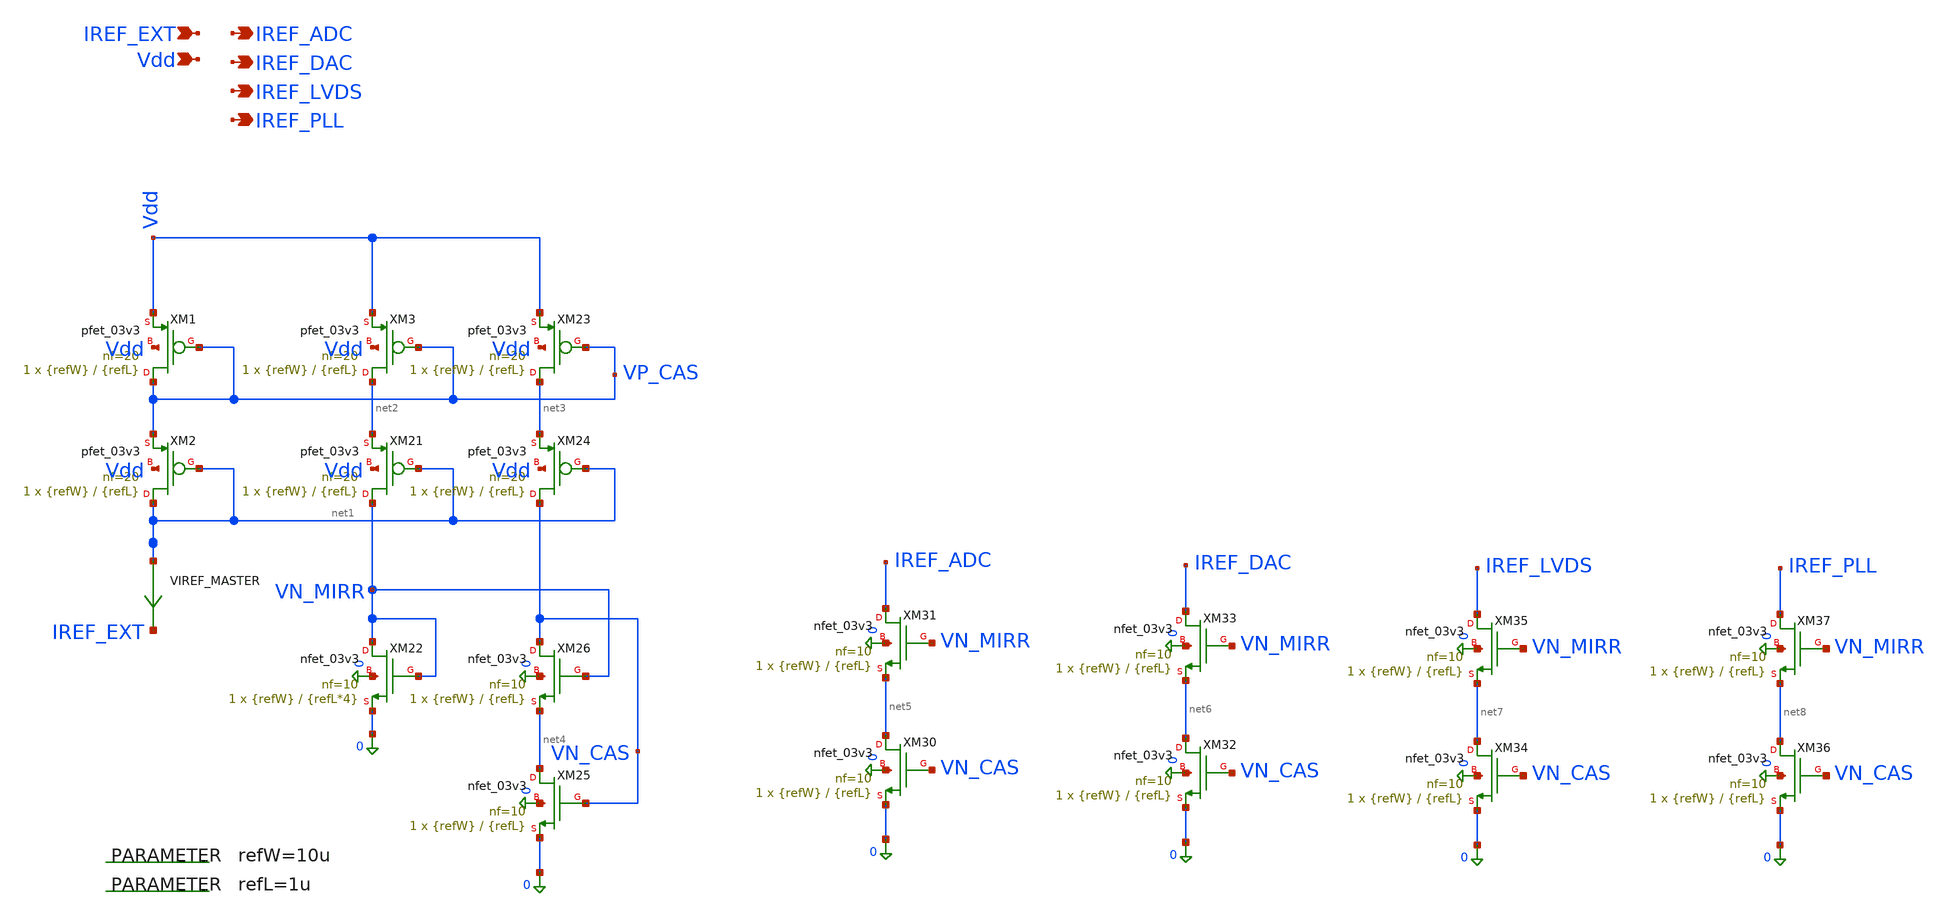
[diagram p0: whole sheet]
** sch_path: blocks/top/iref_master.sch
**.subckt iref_master IREF_ADC IREF_DAC Vdd IREF_EXT IREF_LVDS IREF_PLL
*.opin IREF_ADC
*.opin IREF_DAC
*.ipin Vdd
*.ipin IREF_EXT
*.opin IREF_LVDS
*.opin IREF_PLL
XM1 VP_CAS VP_CAS Vdd Vdd pfet_03v3 L={refL} W={refW} nf=20 ad='int((nf+1)/2) * W/nf * 0.18u' as='int((nf+2)/2) * W/nf * 0.18u'
+ pd='2*int((nf+1)/2) * (W/nf + 0.18u)' ps='2*int((nf+2)/2) * (W/nf + 0.18u)' nrd='0.18u / W' nrs='0.18u / W'
+ sa=0 sb=0 sd=0 m=1
XM2 net1 net1 VP_CAS Vdd pfet_03v3 L={refL} W={refW} nf=20 ad='int((nf+1)/2) * W/nf * 0.18u' as='int((nf+2)/2) * W/nf * 0.18u'
+ pd='2*int((nf+1)/2) * (W/nf + 0.18u)' ps='2*int((nf+2)/2) * (W/nf + 0.18u)' nrd='0.18u / W' nrs='0.18u / W'
+ sa=0 sb=0 sd=0 m=1
XM3 net2 VP_CAS Vdd Vdd pfet_03v3 L={refL} W={refW} nf=20 ad='int((nf+1)/2) * W/nf * 0.18u' as='int((nf+2)/2) * W/nf * 0.18u'
+ pd='2*int((nf+1)/2) * (W/nf + 0.18u)' ps='2*int((nf+2)/2) * (W/nf + 0.18u)' nrd='0.18u / W' nrs='0.18u / W'
+ sa=0 sb=0 sd=0 m=1
XM21 VN_MIRR net1 net2 Vdd pfet_03v3 L={refL} W={refW} nf=20 ad='int((nf+1)/2) * W/nf * 0.18u' as='int((nf+2)/2) * W/nf * 0.18u'
+ pd='2*int((nf+1)/2) * (W/nf + 0.18u)' ps='2*int((nf+2)/2) * (W/nf + 0.18u)' nrd='0.18u / W' nrs='0.18u / W'
+ sa=0 sb=0 sd=0 m=1
XM22 VN_MIRR VN_MIRR 0 0 nfet_03v3 L={refL*4} W={refW} nf=10 ad='int((nf+1)/2) * W/nf * 0.18u' as='int((nf+2)/2) * W/nf * 0.18u'
+ pd='2*int((nf+1)/2) * (W/nf + 0.18u)' ps='2*int((nf+2)/2) * (W/nf + 0.18u)' nrd='0.18u / W' nrs='0.18u / W'
+ sa=0 sb=0 sd=0 m=1
XM23 net3 VP_CAS Vdd Vdd pfet_03v3 L={refL} W={refW} nf=20 ad='int((nf+1)/2) * W/nf * 0.18u' as='int((nf+2)/2) * W/nf * 0.18u'
+ pd='2*int((nf+1)/2) * (W/nf + 0.18u)' ps='2*int((nf+2)/2) * (W/nf + 0.18u)' nrd='0.18u / W' nrs='0.18u / W'
+ sa=0 sb=0 sd=0 m=1
XM24 VN_CAS net1 net3 Vdd pfet_03v3 L={refL} W={refW} nf=20 ad='int((nf+1)/2) * W/nf * 0.18u' as='int((nf+2)/2) * W/nf * 0.18u'
+ pd='2*int((nf+1)/2) * (W/nf + 0.18u)' ps='2*int((nf+2)/2) * (W/nf + 0.18u)' nrd='0.18u / W' nrs='0.18u / W'
+ sa=0 sb=0 sd=0 m=1
XM25 net4 VN_CAS 0 0 nfet_03v3 L={refL} W={refW} nf=10 ad='int((nf+1)/2) * W/nf * 0.18u' as='int((nf+2)/2) * W/nf * 0.18u'
+ pd='2*int((nf+1)/2) * (W/nf + 0.18u)' ps='2*int((nf+2)/2) * (W/nf + 0.18u)' nrd='0.18u / W' nrs='0.18u / W'
+ sa=0 sb=0 sd=0 m=1
XM26 VN_CAS VN_MIRR net4 0 nfet_03v3 L={refL} W={refW} nf=10 ad='int((nf+1)/2) * W/nf * 0.18u' as='int((nf+2)/2) * W/nf * 0.18u'
+ pd='2*int((nf+1)/2) * (W/nf + 0.18u)' ps='2*int((nf+2)/2) * (W/nf + 0.18u)' nrd='0.18u / W' nrs='0.18u / W'
+ sa=0 sb=0 sd=0 m=1
.param refW=10u
.param refL=1u
VIREF_MASTER net1 IREF_EXT 0
.save i(viref_master)
XM30 net5 VN_CAS 0 0 nfet_03v3 L={refL} W={refW} nf=10 ad='int((nf+1)/2) * W/nf * 0.18u' as='int((nf+2)/2) * W/nf * 0.18u'
+ pd='2*int((nf+1)/2) * (W/nf + 0.18u)' ps='2*int((nf+2)/2) * (W/nf + 0.18u)' nrd='0.18u / W' nrs='0.18u / W'
+ sa=0 sb=0 sd=0 m=1
XM31 IREF_ADC VN_MIRR net5 0 nfet_03v3 L={refL} W={refW} nf=10 ad='int((nf+1)/2) * W/nf * 0.18u' as='int((nf+2)/2) * W/nf * 0.18u'
+ pd='2*int((nf+1)/2) * (W/nf + 0.18u)' ps='2*int((nf+2)/2) * (W/nf + 0.18u)' nrd='0.18u / W' nrs='0.18u / W'
+ sa=0 sb=0 sd=0 m=1
XM32 net6 VN_CAS 0 0 nfet_03v3 L={refL} W={refW} nf=10 ad='int((nf+1)/2) * W/nf * 0.18u' as='int((nf+2)/2) * W/nf * 0.18u'
+ pd='2*int((nf+1)/2) * (W/nf + 0.18u)' ps='2*int((nf+2)/2) * (W/nf + 0.18u)' nrd='0.18u / W' nrs='0.18u / W'
+ sa=0 sb=0 sd=0 m=1
XM33 IREF_DAC VN_MIRR net6 0 nfet_03v3 L={refL} W={refW} nf=10 ad='int((nf+1)/2) * W/nf * 0.18u' as='int((nf+2)/2) * W/nf * 0.18u'
+ pd='2*int((nf+1)/2) * (W/nf + 0.18u)' ps='2*int((nf+2)/2) * (W/nf + 0.18u)' nrd='0.18u / W' nrs='0.18u / W'
+ sa=0 sb=0 sd=0 m=1
XM34 net7 VN_CAS 0 0 nfet_03v3 L={refL} W={refW} nf=10 ad='int((nf+1)/2) * W/nf * 0.18u' as='int((nf+2)/2) * W/nf * 0.18u'
+ pd='2*int((nf+1)/2) * (W/nf + 0.18u)' ps='2*int((nf+2)/2) * (W/nf + 0.18u)' nrd='0.18u / W' nrs='0.18u / W'
+ sa=0 sb=0 sd=0 m=1
XM35 IREF_LVDS VN_MIRR net7 0 nfet_03v3 L={refL} W={refW} nf=10 ad='int((nf+1)/2) * W/nf * 0.18u' as='int((nf+2)/2) * W/nf * 0.18u'
+ pd='2*int((nf+1)/2) * (W/nf + 0.18u)' ps='2*int((nf+2)/2) * (W/nf + 0.18u)' nrd='0.18u / W' nrs='0.18u / W'
+ sa=0 sb=0 sd=0 m=1
XM36 net8 VN_CAS 0 0 nfet_03v3 L={refL} W={refW} nf=10 ad='int((nf+1)/2) * W/nf * 0.18u' as='int((nf+2)/2) * W/nf * 0.18u'
+ pd='2*int((nf+1)/2) * (W/nf + 0.18u)' ps='2*int((nf+2)/2) * (W/nf + 0.18u)' nrd='0.18u / W' nrs='0.18u / W'
+ sa=0 sb=0 sd=0 m=1
XM37 IREF_PLL VN_MIRR net8 0 nfet_03v3 L={refL} W={refW} nf=10 ad='int((nf+1)/2) * W/nf * 0.18u' as='int((nf+2)/2) * W/nf * 0.18u'
+ pd='2*int((nf+1)/2) * (W/nf + 0.18u)' ps='2*int((nf+2)/2) * (W/nf + 0.18u)' nrd='0.18u / W' nrs='0.18u / W'
+ sa=0 sb=0 sd=0 m=1
**.ends
.end
